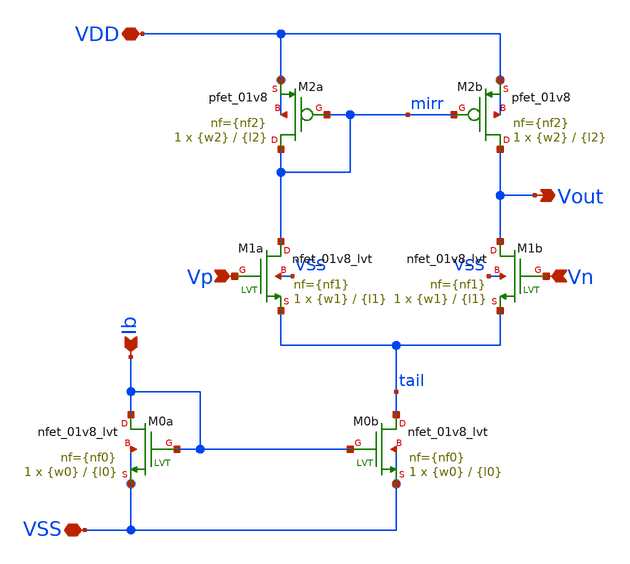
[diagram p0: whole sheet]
** sch_path: ota-5t/xschem/ota-5t.sch
**.subckt ota-5t Vp Vn Vout VDD VSS Ib
*.ipin Vp
*.ipin Vn
*.opin Vout
*.iopin VDD
*.iopin VSS
*.ipin Ib
XM2b Vout mirr VDD VDD sky130_fd_pr__pfet_01v8 L={l2} W={w2} nf={nf2} ad='int((nf+1)/2) * W/nf * 0.29'
+ as='int((nf+2)/2) * W/nf * 0.29' pd='2*int((nf+1)/2) * (W/nf + 0.29)' ps='2*int((nf+2)/2) * (W/nf + 0.29)'
+ nrd='0.29 / W' nrs='0.29 / W' sa=0 sb=0 sd=0 mult=1 m=1
XM2a mirr mirr VDD VDD sky130_fd_pr__pfet_01v8 L={l2} W={w2} nf={nf2} ad='int((nf+1)/2) * W/nf * 0.29'
+ as='int((nf+2)/2) * W/nf * 0.29' pd='2*int((nf+1)/2) * (W/nf + 0.29)' ps='2*int((nf+2)/2) * (W/nf + 0.29)'
+ nrd='0.29 / W' nrs='0.29 / W' sa=0 sb=0 sd=0 mult=1 m=1
XM1a mirr Vp tail VSS sky130_fd_pr__nfet_01v8_lvt L={l1} W={w1} nf={nf1} ad='int((nf+1)/2) * W/nf * 0.29'
+ as='int((nf+2)/2) * W/nf * 0.29' pd='2*int((nf+1)/2) * (W/nf + 0.29)' ps='2*int((nf+2)/2) * (W/nf + 0.29)'
+ nrd='0.29 / W' nrs='0.29 / W' sa=0 sb=0 sd=0 mult=1 m=1
XM1b Vout Vn tail VSS sky130_fd_pr__nfet_01v8_lvt L={l1} W={w1} nf={nf1} ad='int((nf+1)/2) * W/nf * 0.29'
+ as='int((nf+2)/2) * W/nf * 0.29' pd='2*int((nf+1)/2) * (W/nf + 0.29)' ps='2*int((nf+2)/2) * (W/nf + 0.29)'
+ nrd='0.29 / W' nrs='0.29 / W' sa=0 sb=0 sd=0 mult=1 m=1
XM0b tail Ib VSS VSS sky130_fd_pr__nfet_01v8_lvt L={l0} W={w0} nf={nf0} ad='int((nf+1)/2) * W/nf * 0.29'
+ as='int((nf+2)/2) * W/nf * 0.29' pd='2*int((nf+1)/2) * (W/nf + 0.29)' ps='2*int((nf+2)/2) * (W/nf + 0.29)'
+ nrd='0.29 / W' nrs='0.29 / W' sa=0 sb=0 sd=0 mult=1 m=1
XM0a Ib Ib VSS VSS sky130_fd_pr__nfet_01v8_lvt L={l0} W={w0} nf={nf0} ad='int((nf+1)/2) * W/nf * 0.29'
+ as='int((nf+2)/2) * W/nf * 0.29' pd='2*int((nf+1)/2) * (W/nf + 0.29)' ps='2*int((nf+2)/2) * (W/nf + 0.29)'
+ nrd='0.29 / W' nrs='0.29 / W' sa=0 sb=0 sd=0 mult=1 m=1
**.ends
.end
